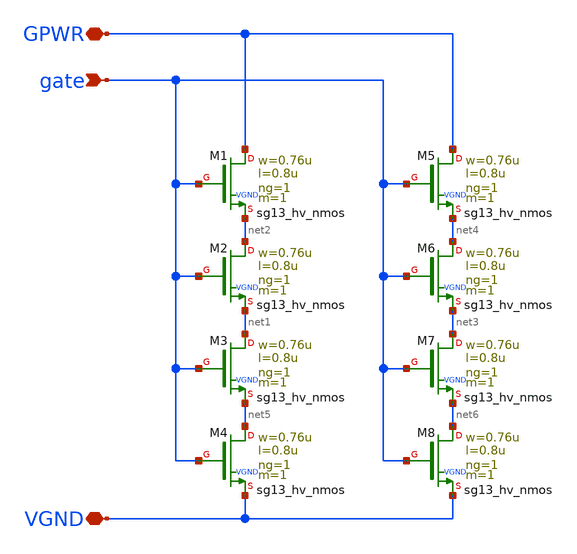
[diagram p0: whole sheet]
** sch_path: pg/ihp-sg13cmos5l/tt_pg_3v3_2/xschem/discharge_3v3.sch
**.subckt discharge_3v3 GPWR VGND gate
*.iopin GPWR
*.iopin VGND
*.ipin gate
XM1 GPWR gate net2 VGND sg13_hv_nmos w=0.76u l=0.8u ng=1 m=1
XM2 net2 gate net1 VGND sg13_hv_nmos w=0.76u l=0.8u ng=1 m=1
XM3 net1 gate net5 VGND sg13_hv_nmos w=0.76u l=0.8u ng=1 m=1
XM4 net5 gate VGND VGND sg13_hv_nmos w=0.76u l=0.8u ng=1 m=1
XM5 GPWR gate net4 VGND sg13_hv_nmos w=0.76u l=0.8u ng=1 m=1
XM6 net4 gate net3 VGND sg13_hv_nmos w=0.76u l=0.8u ng=1 m=1
XM7 net3 gate net6 VGND sg13_hv_nmos w=0.76u l=0.8u ng=1 m=1
XM8 net6 gate VGND VGND sg13_hv_nmos w=0.76u l=0.8u ng=1 m=1
**.ends
.end
